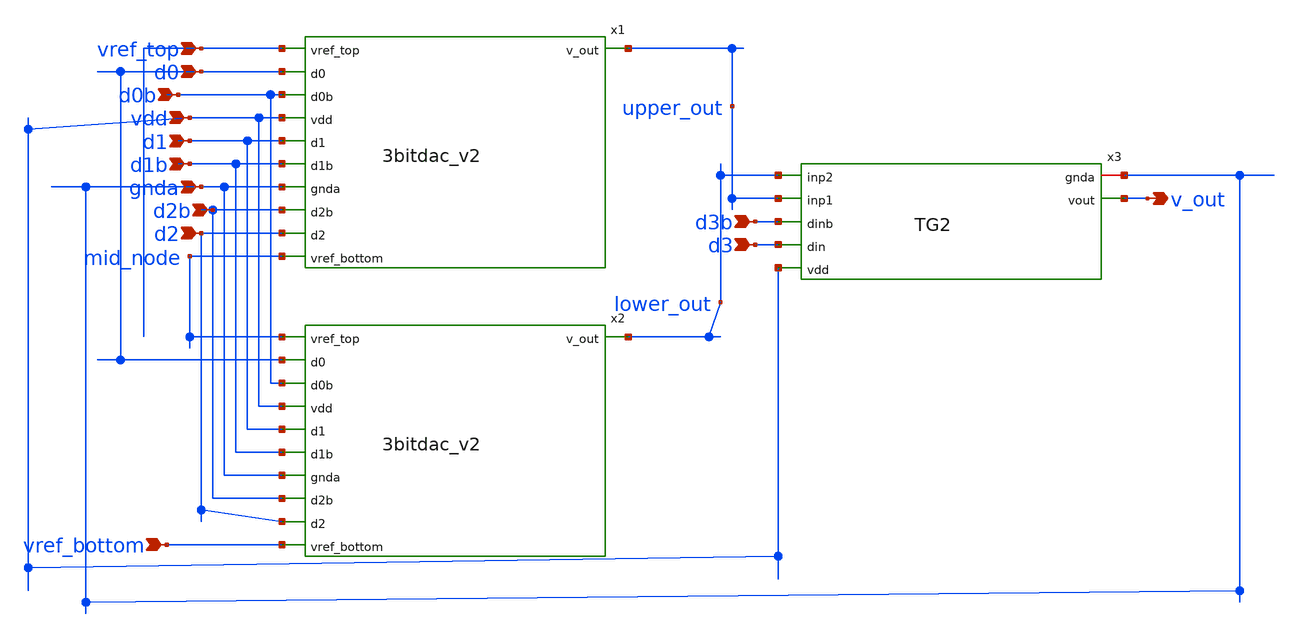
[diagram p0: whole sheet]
** sch_path: prelayout/4bitdac_v2.sch
**.subckt 4bitdac_v2 vref_top gnda vdd d3 d3b d2 d2b d1 d1b d0 d0b v_out vref_bottom
*.ipin vref_top
*.ipin gnda
*.ipin vdd
*.ipin d3
*.ipin d3b
*.ipin d2
*.ipin d2b
*.ipin d1
*.ipin d1b
*.ipin d0
*.ipin d0b
*.opin v_out
*.ipin vref_bottom
Xx3 gnda v_out lower_out upper_out d3b d3 vdd TG2
x1 vref_top d0 d0b vdd d1 d1b upper_out gnda d2b d2 mid_node 3bitdac_v2
x2 mid_node d0 d0b vdd d1 d1b lower_out gnda d2b d2 vref_bottom 3bitdac_v2
**.ends
.end
